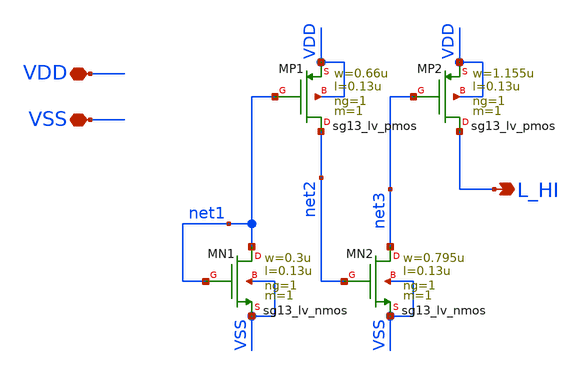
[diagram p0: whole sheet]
** sch_path: xschem/sg13g2_tiehi.sch
**.subckt sg13g2_tiehi VSS VDD L_HI
*.iopin VSS
*.iopin VDD
*.opin L_HI
XMN1 net1 net1 VSS VSS sg13_lv_nmos w=0.3u l=0.13u ng=1 m=1 mm_ok=1
XMP1 net2 net1 VDD VDD sg13_lv_pmos w=0.66u l=0.13u ng=1 m=1 mm_ok=1
XMN2 net3 net2 VSS VSS sg13_lv_nmos w=0.795u l=0.13u ng=1 m=1 mm_ok=1
XMP2 L_HI net3 VDD VDD sg13_lv_pmos w=1.155u l=0.13u ng=1 m=1 mm_ok=1
**.ends
.end
